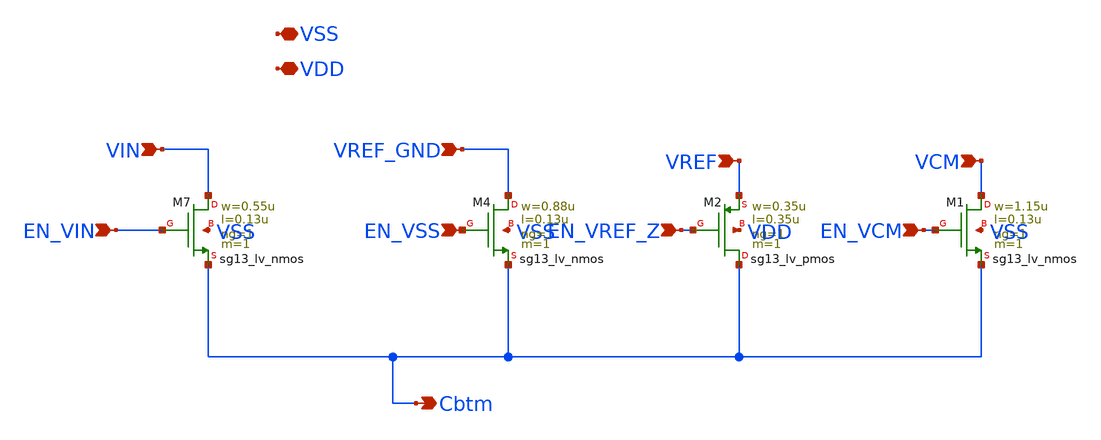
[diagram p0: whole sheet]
** sch_path: schematic/individual_switches/switch_C5.sch
**.subckt switch_C5 VIN EN_VIN VREF_GND EN_VSS Cbtm VSS VREF EN_VREF_Z EN_VCM VCM VDD
*.ipin VIN
*.ipin EN_VIN
*.ipin VREF_GND
*.ipin EN_VSS
*.opin Cbtm
*.iopin VSS
*.ipin VREF
*.ipin EN_VREF_Z
*.ipin EN_VCM
*.ipin VCM
*.iopin VDD
XM7 VIN EN_VIN Cbtm VSS sg13_lv_nmos w=0.55u l=0.13u ng=1 m=1 mm_ok=1
XM1 VCM EN_VCM Cbtm VSS sg13_lv_nmos w=1.15u l=0.13u ng=1 m=1 mm_ok=1
XM2 Cbtm EN_VREF_Z VREF VDD sg13_lv_pmos w=0.35u l=0.35u ng=1 m=1 mm_ok=1
XM4 VREF_GND EN_VSS Cbtm VSS sg13_lv_nmos w=0.88u l=0.13u ng=1 m=1 mm_ok=1
**.ends
.end
